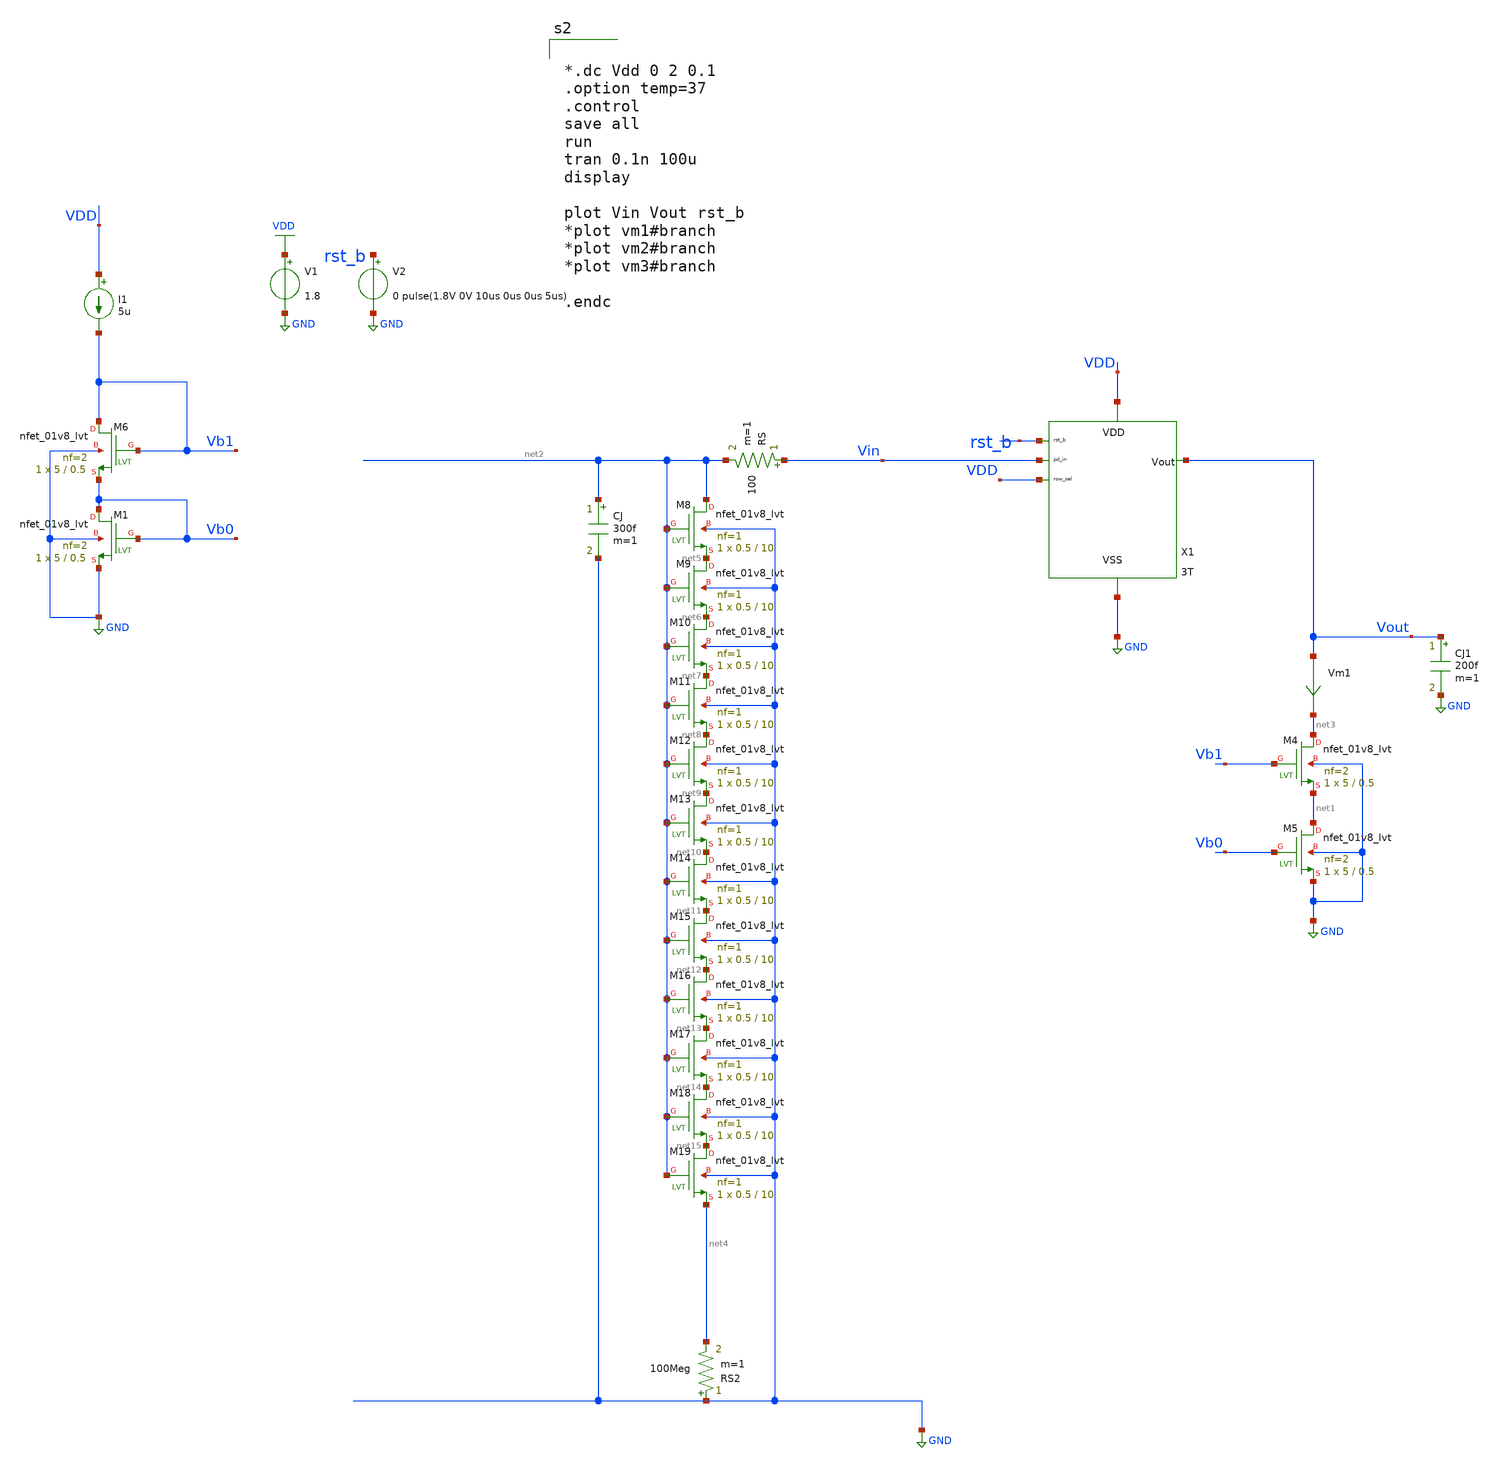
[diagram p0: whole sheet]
** sch_path: xschem/cmos_imager/tb_pixel2.sch
**.subckt tb_pixel2
XM4 net3 Vb1 net1 GND sky130_fd_pr__nfet_01v8_lvt L=0.5 W=5 nf=2 ad='int((nf+1)/2) * W/nf * 0.29' as='int((nf+2)/2) * W/nf * 0.29'
+ pd='2*int((nf+1)/2) * (W/nf + 0.29)' ps='2*int((nf+2)/2) * (W/nf + 0.29)' nrd='0.29 / W' nrs='0.29 / W'
+ sa=0 sb=0 sd=0 mult=1 m=1
XM5 net1 Vb0 GND GND sky130_fd_pr__nfet_01v8_lvt L=0.5 W=5 nf=2 ad='int((nf+1)/2) * W/nf * 0.29' as='int((nf+2)/2) * W/nf * 0.29'
+ pd='2*int((nf+1)/2) * (W/nf + 0.29)' ps='2*int((nf+2)/2) * (W/nf + 0.29)' nrd='0.29 / W' nrs='0.29 / W'
+ sa=0 sb=0 sd=0 mult=1 m=1
CJ net2 GND 300f m=1
RS Vin net2 100 m=1
XM6 Vb1 Vb1 Vb0 GND sky130_fd_pr__nfet_01v8_lvt L=0.5 W=5 nf=2 ad='int((nf+1)/2) * W/nf * 0.29' as='int((nf+2)/2) * W/nf * 0.29'
+ pd='2*int((nf+1)/2) * (W/nf + 0.29)' ps='2*int((nf+2)/2) * (W/nf + 0.29)' nrd='0.29 / W' nrs='0.29 / W'
+ sa=0 sb=0 sd=0 mult=1 m=1
XM1 Vb0 Vb0 GND GND sky130_fd_pr__nfet_01v8_lvt L=0.5 W=5 nf=2 ad='int((nf+1)/2) * W/nf * 0.29' as='int((nf+2)/2) * W/nf * 0.29'
+ pd='2*int((nf+1)/2) * (W/nf + 0.29)' ps='2*int((nf+2)/2) * (W/nf + 0.29)' nrd='0.29 / W' nrs='0.29 / W'
+ sa=0 sb=0 sd=0 mult=1 m=1
I1 VDD Vb1 5u
V1 VDD GND 1.8
Vm1 Vout net3 0
.save i(vm1)
V2 rst_b GND 0 pulse(1.8V 0V 10us 0us 0us 5us)
CJ1 Vout GND 200f m=1
XM8 net2 net2 net5 GND sky130_fd_pr__nfet_01v8_lvt L=10 W=0.5 nf=1 ad='int((nf+1)/2) * W/nf * 0.29' as='int((nf+2)/2) * W/nf * 0.29'
+ pd='2*int((nf+1)/2) * (W/nf + 0.29)' ps='2*int((nf+2)/2) * (W/nf + 0.29)' nrd='0.29 / W' nrs='0.29 / W'
+ sa=0 sb=0 sd=0 mult=1 m=1
XM9 net5 net2 net6 GND sky130_fd_pr__nfet_01v8_lvt L=10 W=0.5 nf=1 ad='int((nf+1)/2) * W/nf * 0.29' as='int((nf+2)/2) * W/nf * 0.29'
+ pd='2*int((nf+1)/2) * (W/nf + 0.29)' ps='2*int((nf+2)/2) * (W/nf + 0.29)' nrd='0.29 / W' nrs='0.29 / W'
+ sa=0 sb=0 sd=0 mult=1 m=1
XM10 net6 net2 net7 GND sky130_fd_pr__nfet_01v8_lvt L=10 W=0.5 nf=1 ad='int((nf+1)/2) * W/nf * 0.29'
+ as='int((nf+2)/2) * W/nf * 0.29' pd='2*int((nf+1)/2) * (W/nf + 0.29)' ps='2*int((nf+2)/2) * (W/nf + 0.29)'
+ nrd='0.29 / W' nrs='0.29 / W' sa=0 sb=0 sd=0 mult=1 m=1
XM11 net7 net2 net8 GND sky130_fd_pr__nfet_01v8_lvt L=10 W=0.5 nf=1 ad='int((nf+1)/2) * W/nf * 0.29'
+ as='int((nf+2)/2) * W/nf * 0.29' pd='2*int((nf+1)/2) * (W/nf + 0.29)' ps='2*int((nf+2)/2) * (W/nf + 0.29)'
+ nrd='0.29 / W' nrs='0.29 / W' sa=0 sb=0 sd=0 mult=1 m=1
XM12 net8 net2 net9 GND sky130_fd_pr__nfet_01v8_lvt L=10 W=0.5 nf=1 ad='int((nf+1)/2) * W/nf * 0.29'
+ as='int((nf+2)/2) * W/nf * 0.29' pd='2*int((nf+1)/2) * (W/nf + 0.29)' ps='2*int((nf+2)/2) * (W/nf + 0.29)'
+ nrd='0.29 / W' nrs='0.29 / W' sa=0 sb=0 sd=0 mult=1 m=1
XM13 net9 net2 net10 GND sky130_fd_pr__nfet_01v8_lvt L=10 W=0.5 nf=1 ad='int((nf+1)/2) * W/nf * 0.29'
+ as='int((nf+2)/2) * W/nf * 0.29' pd='2*int((nf+1)/2) * (W/nf + 0.29)' ps='2*int((nf+2)/2) * (W/nf + 0.29)'
+ nrd='0.29 / W' nrs='0.29 / W' sa=0 sb=0 sd=0 mult=1 m=1
XM14 net10 net2 net11 GND sky130_fd_pr__nfet_01v8_lvt L=10 W=0.5 nf=1 ad='int((nf+1)/2) * W/nf * 0.29'
+ as='int((nf+2)/2) * W/nf * 0.29' pd='2*int((nf+1)/2) * (W/nf + 0.29)' ps='2*int((nf+2)/2) * (W/nf + 0.29)'
+ nrd='0.29 / W' nrs='0.29 / W' sa=0 sb=0 sd=0 mult=1 m=1
XM15 net11 net2 net12 GND sky130_fd_pr__nfet_01v8_lvt L=10 W=0.5 nf=1 ad='int((nf+1)/2) * W/nf * 0.29'
+ as='int((nf+2)/2) * W/nf * 0.29' pd='2*int((nf+1)/2) * (W/nf + 0.29)' ps='2*int((nf+2)/2) * (W/nf + 0.29)'
+ nrd='0.29 / W' nrs='0.29 / W' sa=0 sb=0 sd=0 mult=1 m=1
XM16 net12 net2 net13 GND sky130_fd_pr__nfet_01v8_lvt L=10 W=0.5 nf=1 ad='int((nf+1)/2) * W/nf * 0.29'
+ as='int((nf+2)/2) * W/nf * 0.29' pd='2*int((nf+1)/2) * (W/nf + 0.29)' ps='2*int((nf+2)/2) * (W/nf + 0.29)'
+ nrd='0.29 / W' nrs='0.29 / W' sa=0 sb=0 sd=0 mult=1 m=1
XM17 net13 net2 net14 GND sky130_fd_pr__nfet_01v8_lvt L=10 W=0.5 nf=1 ad='int((nf+1)/2) * W/nf * 0.29'
+ as='int((nf+2)/2) * W/nf * 0.29' pd='2*int((nf+1)/2) * (W/nf + 0.29)' ps='2*int((nf+2)/2) * (W/nf + 0.29)'
+ nrd='0.29 / W' nrs='0.29 / W' sa=0 sb=0 sd=0 mult=1 m=1
XM18 net14 net2 net15 GND sky130_fd_pr__nfet_01v8_lvt L=10 W=0.5 nf=1 ad='int((nf+1)/2) * W/nf * 0.29'
+ as='int((nf+2)/2) * W/nf * 0.29' pd='2*int((nf+1)/2) * (W/nf + 0.29)' ps='2*int((nf+2)/2) * (W/nf + 0.29)'
+ nrd='0.29 / W' nrs='0.29 / W' sa=0 sb=0 sd=0 mult=1 m=1
XM19 net15 net2 net4 GND sky130_fd_pr__nfet_01v8_lvt L=10 W=0.5 nf=1 ad='int((nf+1)/2) * W/nf * 0.29'
+ as='int((nf+2)/2) * W/nf * 0.29' pd='2*int((nf+1)/2) * (W/nf + 0.29)' ps='2*int((nf+2)/2) * (W/nf + 0.29)'
+ nrd='0.29 / W' nrs='0.29 / W' sa=0 sb=0 sd=0 mult=1 m=1
RS2 GND net4 100Meg m=1
X1 VDD Vin rst_b VDD GND Vout 3T
**** begin user architecture code

** opencircuitdesign pdks install
.lib $::SKYWATER_MODELS/sky130.lib.spice tt




*.dc Vdd 0 2 0.1
.option temp=37
.control
save all
run
tran 0.1n 100u
display

plot Vin Vout rst_b
*plot vm1#branch
*plot vm2#branch
*plot vm3#branch

.endc


**** end user architecture code
**.ends

* expanding   symbol:  cmos_imager/3T.sym # of pins=6
** sym_path: xschem/cmos_imager/3T.sym
** sch_path: xschem/cmos_imager/3T.sch
.subckt 3T row_sel pd_in rst_b VDD VSS Vout
*.opin Vout
*.ipin rst_b
*.ipin pd_in
*.iopin VDD
*.ipin row_sel
*.iopin VSS
XM2 net2 pd_in net1 VSS sky130_fd_pr__nfet_01v8_lvt L=0.5 W=1 nf=1 ad='int((nf+1)/2) * W/nf * 0.29' as='int((nf+2)/2) * W/nf * 0.29'
+ pd='2*int((nf+1)/2) * (W/nf + 0.29)' ps='2*int((nf+2)/2) * (W/nf + 0.29)' nrd='0.29 / W' nrs='0.29 / W'
+ sa=0 sb=0 sd=0 mult=10 m=10
Vm2 net1 Vmid 0
.save i(vm2)
Vm3 VDD net2 0
.save i(vm3)
XM3 Vmid row_sel Vout VSS sky130_fd_pr__nfet_01v8_lvt L=0.5 W=1 nf=1 ad='int((nf+1)/2) * W/nf * 0.29'
+ as='int((nf+2)/2) * W/nf * 0.29' pd='2*int((nf+1)/2) * (W/nf + 0.29)' ps='2*int((nf+2)/2) * (W/nf + 0.29)'
+ nrd='0.29 / W' nrs='0.29 / W' sa=0 sb=0 sd=0 mult=20 m=20
XM20 pd_in rst_b VDD VDD sky130_fd_pr__pfet_01v8 L=0.5 W=1 nf=1 ad='int((nf+1)/2) * W/nf * 0.29' as='int((nf+2)/2) * W/nf * 0.29'
+ pd='2*int((nf+1)/2) * (W/nf + 0.29)' ps='2*int((nf+2)/2) * (W/nf + 0.29)' nrd='0.29 / W' nrs='0.29 / W'
+ sa=0 sb=0 sd=0 mult=1 m=1
.ends

.GLOBAL GND
.GLOBAL VDD
.end
